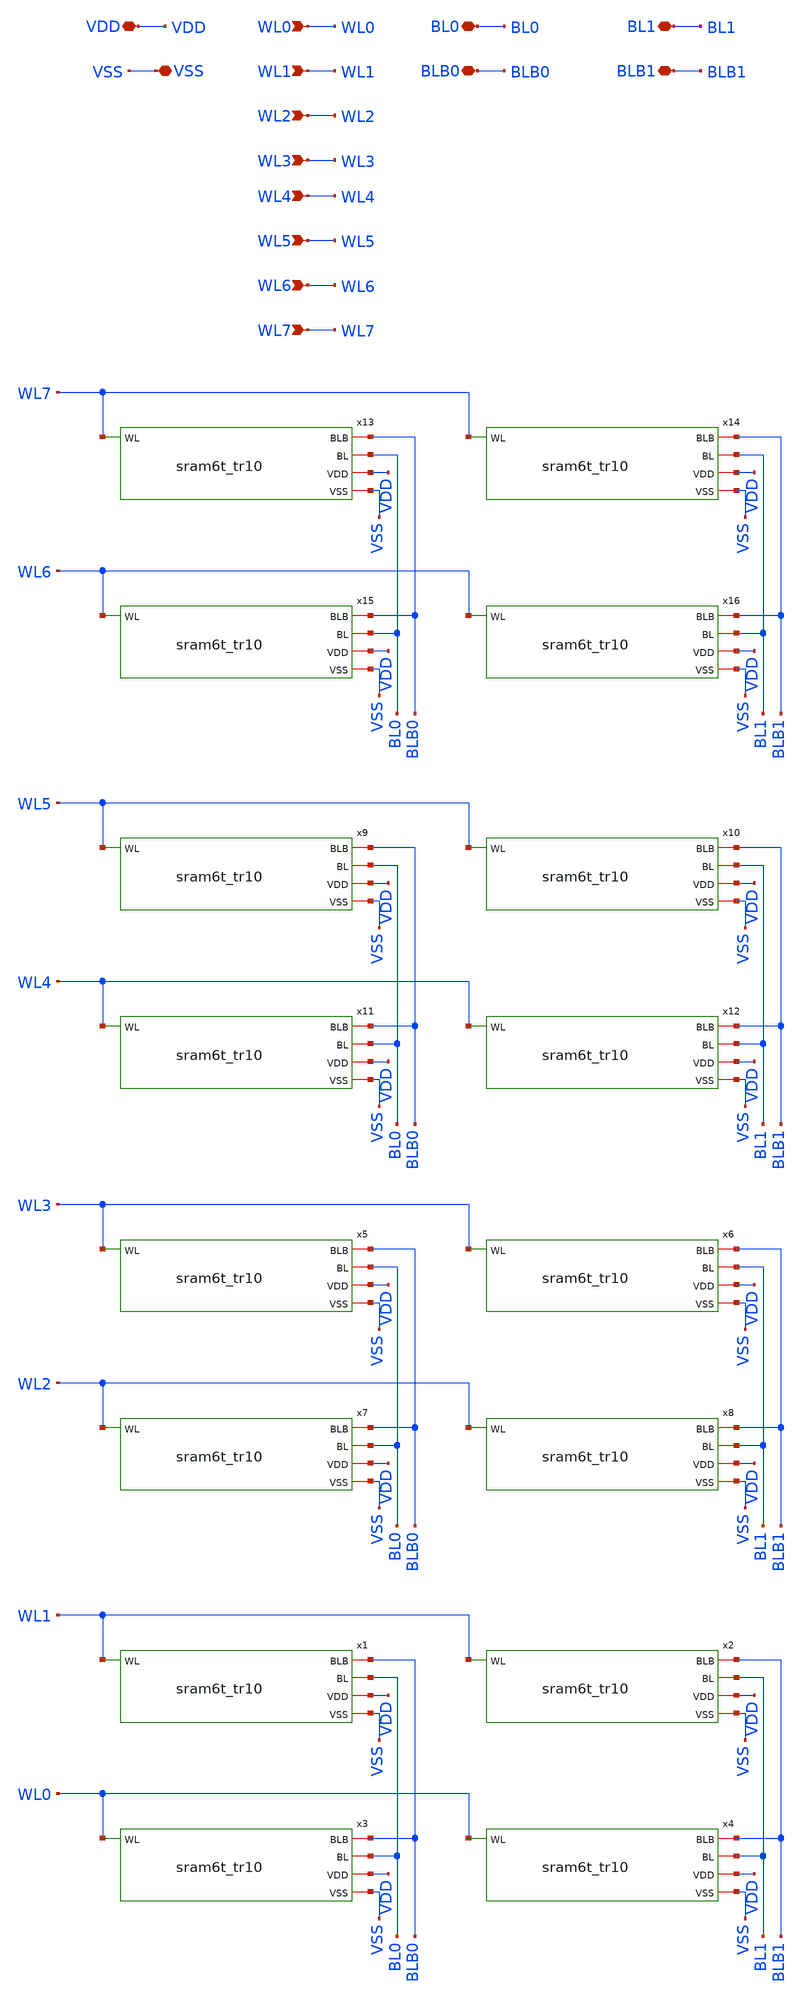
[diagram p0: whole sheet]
** sch_path: array/8word_x_2bit_test/sram_8w2b.sch
**.subckt sram_8w2b VDD VSS BL0 BLB0 BL1 BLB1 WL0 WL1 WL2 WL3 WL4 WL5 WL6 WL7
*.iopin VDD
*.iopin VSS
*.iopin BL0
*.iopin BLB0
*.iopin BL1
*.iopin BLB1
*.ipin WL0
*.ipin WL1
*.ipin WL2
*.ipin WL3
*.ipin WL4
*.ipin WL5
*.ipin WL6
*.ipin WL7
x1 BL0 BLB0 WL1 VDD VSS sram6t_tr10
x2 BL1 BLB1 WL1 VDD VSS sram6t_tr10
x3 BL0 BLB0 WL0 VDD VSS sram6t_tr10
x4 BL1 BLB1 WL0 VDD VSS sram6t_tr10
x5 BL0 BLB0 WL3 VDD VSS sram6t_tr10
x6 BL1 BLB1 WL3 VDD VSS sram6t_tr10
x7 BL0 BLB0 WL2 VDD VSS sram6t_tr10
x8 BL1 BLB1 WL2 VDD VSS sram6t_tr10
x9 BL0 BLB0 WL5 VDD VSS sram6t_tr10
x10 BL1 BLB1 WL5 VDD VSS sram6t_tr10
x11 BL0 BLB0 WL4 VDD VSS sram6t_tr10
x12 BL1 BLB1 WL4 VDD VSS sram6t_tr10
x13 BL0 BLB0 WL7 VDD VSS sram6t_tr10
x14 BL1 BLB1 WL7 VDD VSS sram6t_tr10
x15 BL0 BLB0 WL6 VDD VSS sram6t_tr10
x16 BL1 BLB1 WL6 VDD VSS sram6t_tr10
**.ends
.end
